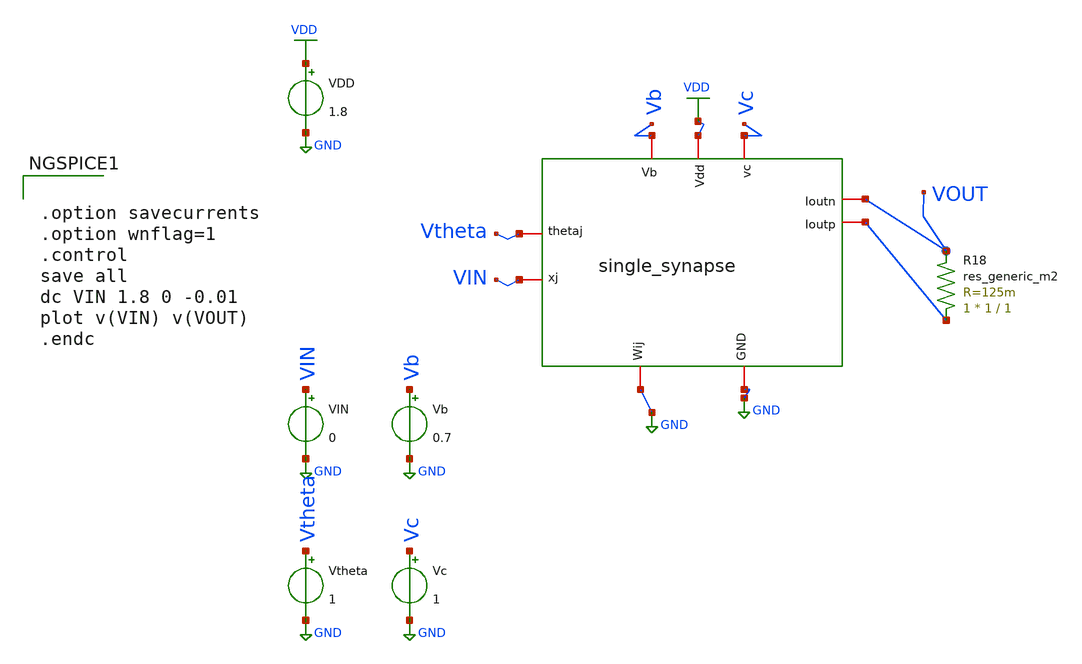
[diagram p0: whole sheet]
** sch_path: test_single_synapse.sch
**.subckt test_single_synapse
x1 VDD VOUT net1 VIN Vtheta Vc GND Vb GND single_synapse
VDD VDD GND 1.8
VIN VIN GND 0
R18 net1 VOUT sky130_fd_pr__res_generic_m2 W=1 L=1 m=1
Vb Vb GND 0.7
Vtheta Vtheta GND 1
Vc Vc GND 1
**** begin user architecture code


.option savecurrents
.option wnflag=1
.control
save all
dc VIN 1.8 0 -0.01
plot v(VIN) v(VOUT)
.endc



.option wnflag=1
.lib ~/skywater/skywater-pdk/libraries/sky130_fd_pr_ngspice/latest/models/sky130.lib.spice tt

**** end user architecture code
**.ends
.GLOBAL GND
.GLOBAL VDD
.end
